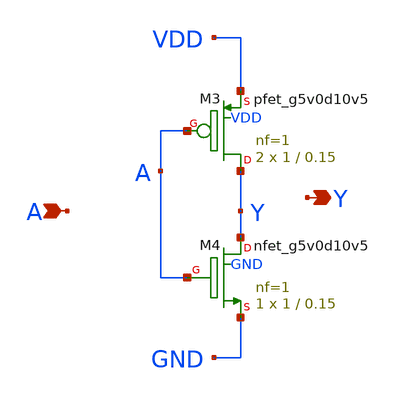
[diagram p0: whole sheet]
** sch_path: lib/xschem/example_inv.sch
**.subckt example_inv Y A
*.opin Y
*.ipin A
XM3 Y A VDD VDD sky130_fd_pr__pfet_g5v0d10v5 L=0.15 W=1 nf=1 ad='int((nf+1)/2) * W/nf * 0.29' as='int((nf+2)/2) * W/nf * 0.29'
+ pd='2*int((nf+1)/2) * (W/nf + 0.29)' ps='2*int((nf+2)/2) * (W/nf + 0.29)' nrd='0.29 / W' nrs='0.29 / W'
+ sa=0 sb=0 sd=0 mult=2 m=2
XM4 Y A GND GND sky130_fd_pr__nfet_g5v0d10v5 L=0.15 W=1 nf=1 ad='int((nf+1)/2) * W/nf * 0.29' as='int((nf+2)/2) * W/nf * 0.29'
+ pd='2*int((nf+1)/2) * (W/nf + 0.29)' ps='2*int((nf+2)/2) * (W/nf + 0.29)' nrd='0.29 / W' nrs='0.29 / W'
+ sa=0 sb=0 sd=0 mult=1 m=1
**.ends
.end
